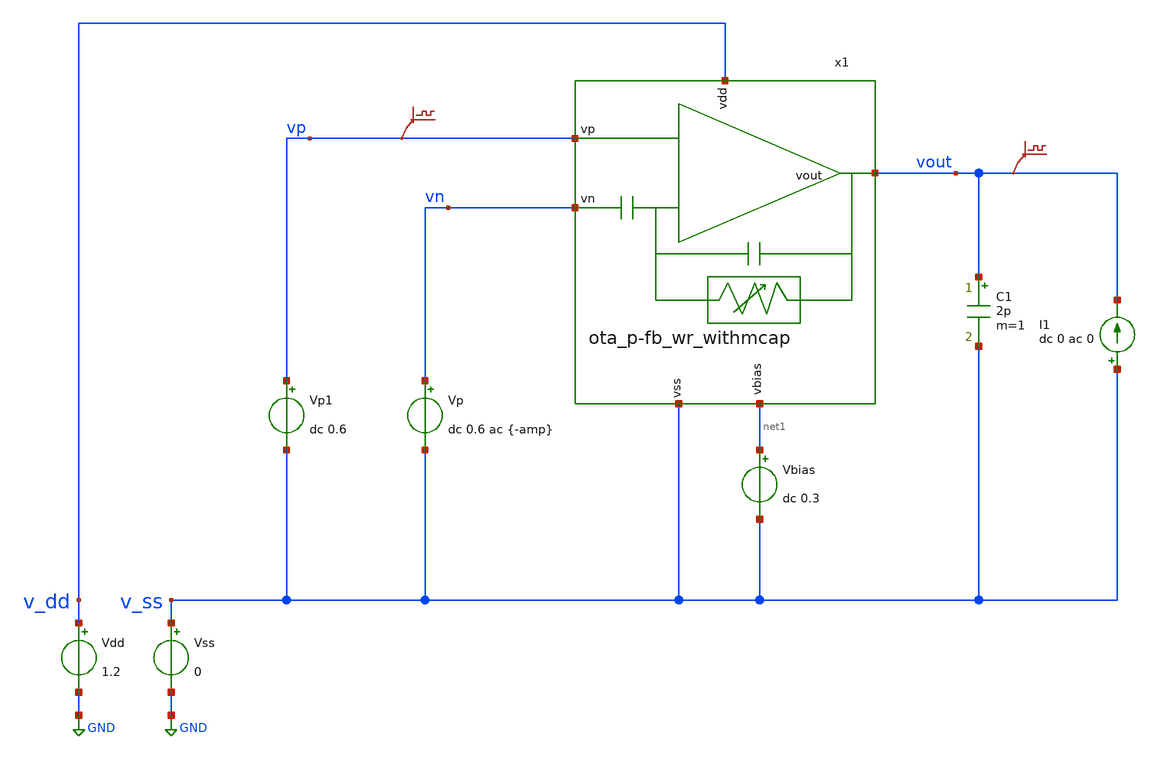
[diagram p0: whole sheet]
** sch_path: v2_feature_extr/ota_p-fb-wr_tb-ac.sch
* (c) 2024-2025 Harald Pretl, Apache-2.0 license
**.subckt ota_p-fb-wr_tb-ac
Vdd v_dd GND 1.2
Vss v_ss GND 0
C1 vout v_ss 2p m=1
.save v(vp)
.save v(vout)
I1 v_ss vout dc 0 ac 0
Vp vn v_ss dc 0.6 ac {-amp}
Vp1 vp v_ss dc 0.6
Vbias net1 v_ss dc 0.3
x1 v_dd vp vout vn v_ss net1 ota_p-fb_wr_withmcap
**** begin user architecture code
 .lib cornerMOSlv.lib mos_ss
.lib cornerMOShv.lib mos_tt
.include $::PDK_ROOT/ihp-sg13cmos5l/libs.tech/ngspice/models/cap_mfringe.lib



.temp 27
.param amp=1
.control
option sparse
save all
op
*write ota_p-fb-wr_tb-ac_SS.raw
set appendwrite

ac dec 101 1m 100MEG
*write  ota_p-fb-wr_tb-ac_SS.raw
plot vp vn
plot 20*log10(vout/(vp-vn))
plot cph(vout/(vp-vn))*180/pi
plot ph(vout/(vp-vn))*180/pi
plot (x1.vin_f - vout) / (i(v.x1.vmeas))

*wrdata ota_p-fb-wr_tb-ac_TT.csv v(vout) v(vp) v(vn) v(x1.vin_f) v(v.x1.vmeas)
*wrdata ota_p-fb-wr_tb-ac_TT.csv gain phase pseudo_res

meas ac dcgain MAX vmag(vout) FROM=1m TO=100k
*let f3db = dcgain/sqrt(2)
*meas ac fbw WHEN vmag(vout)=f3db FALL=1
*let gainerror=(dcgain-1)/1
*print 20*log10(dcgain)
*print gaindb
*print fbw
*print gainerror

noise v(vout) (vp) dec 101 1m 1MEG
print onoise_total
print inoise_total


.endc


**** end user architecture code
**.ends
.GLOBAL GND
.end
